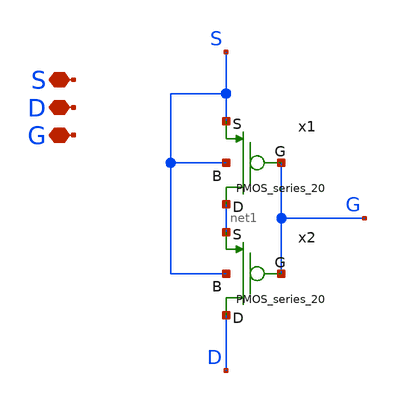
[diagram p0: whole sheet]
** sch_path: Voltage_Reference/symbols_vr/PMOS_series_20_2.sch
**.subckt PMOS_series_20_2 S D G
*.iopin S
*.iopin D
*.iopin G
x1 S net1 S G PMOS_series_20
x2 net1 D S G PMOS_series_20
**.ends

* expanding   symbol:  symbols_vr/PMOS_series_20.sym # of pins=4
** sym_path: Voltage_Reference/symbols_vr/PMOS_series_20.sym
** sch_path: Voltage_Reference/symbols_vr/PMOS_series_20.sch
.subckt PMOS_series_20 S D B G
*.iopin S
*.iopin D
*.iopin B
*.iopin G
XMP1 net1 G S B pfet_03v3 L=2u W=2u nf=1 ad='int((nf+1)/2) * W/nf * 0.18u' as='int((nf+2)/2) * W/nf * 0.18u'
+ pd='2*int((nf+1)/2) * (W/nf + 0.18u)' ps='2*int((nf+2)/2) * (W/nf + 0.18u)' nrd='0.18u / W' nrs='0.18u / W'
+ sa=0 sb=0 sd=0 m=1
XMP2 net3 G net1 B pfet_03v3 L=2u W=2u nf=1 ad='int((nf+1)/2) * W/nf * 0.18u' as='int((nf+2)/2) * W/nf * 0.18u'
+ pd='2*int((nf+1)/2) * (W/nf + 0.18u)' ps='2*int((nf+2)/2) * (W/nf + 0.18u)' nrd='0.18u / W' nrs='0.18u / W'
+ sa=0 sb=0 sd=0 m=1
XMP3 net2 G net3 B pfet_03v3 L=2u W=2u nf=1 ad='int((nf+1)/2) * W/nf * 0.18u' as='int((nf+2)/2) * W/nf * 0.18u'
+ pd='2*int((nf+1)/2) * (W/nf + 0.18u)' ps='2*int((nf+2)/2) * (W/nf + 0.18u)' nrd='0.18u / W' nrs='0.18u / W'
+ sa=0 sb=0 sd=0 m=1
XMP4 net5 G net2 B pfet_03v3 L=2u W=2u nf=1 ad='int((nf+1)/2) * W/nf * 0.18u' as='int((nf+2)/2) * W/nf * 0.18u'
+ pd='2*int((nf+1)/2) * (W/nf + 0.18u)' ps='2*int((nf+2)/2) * (W/nf + 0.18u)' nrd='0.18u / W' nrs='0.18u / W'
+ sa=0 sb=0 sd=0 m=1
XMP5 net4 G net5 B pfet_03v3 L=2u W=2u nf=1 ad='int((nf+1)/2) * W/nf * 0.18u' as='int((nf+2)/2) * W/nf * 0.18u'
+ pd='2*int((nf+1)/2) * (W/nf + 0.18u)' ps='2*int((nf+2)/2) * (W/nf + 0.18u)' nrd='0.18u / W' nrs='0.18u / W'
+ sa=0 sb=0 sd=0 m=1
XMP6 net7 G net4 B pfet_03v3 L=2u W=2u nf=1 ad='int((nf+1)/2) * W/nf * 0.18u' as='int((nf+2)/2) * W/nf * 0.18u'
+ pd='2*int((nf+1)/2) * (W/nf + 0.18u)' ps='2*int((nf+2)/2) * (W/nf + 0.18u)' nrd='0.18u / W' nrs='0.18u / W'
+ sa=0 sb=0 sd=0 m=1
XMP7 net6 G net7 B pfet_03v3 L=2u W=2u nf=1 ad='int((nf+1)/2) * W/nf * 0.18u' as='int((nf+2)/2) * W/nf * 0.18u'
+ pd='2*int((nf+1)/2) * (W/nf + 0.18u)' ps='2*int((nf+2)/2) * (W/nf + 0.18u)' nrd='0.18u / W' nrs='0.18u / W'
+ sa=0 sb=0 sd=0 m=1
XMP8 net9 G net6 B pfet_03v3 L=2u W=2u nf=1 ad='int((nf+1)/2) * W/nf * 0.18u' as='int((nf+2)/2) * W/nf * 0.18u'
+ pd='2*int((nf+1)/2) * (W/nf + 0.18u)' ps='2*int((nf+2)/2) * (W/nf + 0.18u)' nrd='0.18u / W' nrs='0.18u / W'
+ sa=0 sb=0 sd=0 m=1
XMP9 net8 G net9 B pfet_03v3 L=2u W=2u nf=1 ad='int((nf+1)/2) * W/nf * 0.18u' as='int((nf+2)/2) * W/nf * 0.18u'
+ pd='2*int((nf+1)/2) * (W/nf + 0.18u)' ps='2*int((nf+2)/2) * (W/nf + 0.18u)' nrd='0.18u / W' nrs='0.18u / W'
+ sa=0 sb=0 sd=0 m=1
XMP10 net19 G net8 B pfet_03v3 L=2u W=2u nf=1 ad='int((nf+1)/2) * W/nf * 0.18u' as='int((nf+2)/2) * W/nf * 0.18u'
+ pd='2*int((nf+1)/2) * (W/nf + 0.18u)' ps='2*int((nf+2)/2) * (W/nf + 0.18u)' nrd='0.18u / W' nrs='0.18u / W'
+ sa=0 sb=0 sd=0 m=1
XMP11 net10 G net19 B pfet_03v3 L=2u W=2u nf=1 ad='int((nf+1)/2) * W/nf * 0.18u' as='int((nf+2)/2) * W/nf * 0.18u'
+ pd='2*int((nf+1)/2) * (W/nf + 0.18u)' ps='2*int((nf+2)/2) * (W/nf + 0.18u)' nrd='0.18u / W' nrs='0.18u / W'
+ sa=0 sb=0 sd=0 m=1
XMP12 net12 G net10 B pfet_03v3 L=2u W=2u nf=1 ad='int((nf+1)/2) * W/nf * 0.18u' as='int((nf+2)/2) * W/nf * 0.18u'
+ pd='2*int((nf+1)/2) * (W/nf + 0.18u)' ps='2*int((nf+2)/2) * (W/nf + 0.18u)' nrd='0.18u / W' nrs='0.18u / W'
+ sa=0 sb=0 sd=0 m=1
XMP13 net11 G net12 B pfet_03v3 L=2u W=2u nf=1 ad='int((nf+1)/2) * W/nf * 0.18u' as='int((nf+2)/2) * W/nf * 0.18u'
+ pd='2*int((nf+1)/2) * (W/nf + 0.18u)' ps='2*int((nf+2)/2) * (W/nf + 0.18u)' nrd='0.18u / W' nrs='0.18u / W'
+ sa=0 sb=0 sd=0 m=1
XMP14 net14 G net11 B pfet_03v3 L=2u W=2u nf=1 ad='int((nf+1)/2) * W/nf * 0.18u' as='int((nf+2)/2) * W/nf * 0.18u'
+ pd='2*int((nf+1)/2) * (W/nf + 0.18u)' ps='2*int((nf+2)/2) * (W/nf + 0.18u)' nrd='0.18u / W' nrs='0.18u / W'
+ sa=0 sb=0 sd=0 m=1
XMP15 net13 G net14 B pfet_03v3 L=2u W=2u nf=1 ad='int((nf+1)/2) * W/nf * 0.18u' as='int((nf+2)/2) * W/nf * 0.18u'
+ pd='2*int((nf+1)/2) * (W/nf + 0.18u)' ps='2*int((nf+2)/2) * (W/nf + 0.18u)' nrd='0.18u / W' nrs='0.18u / W'
+ sa=0 sb=0 sd=0 m=1
XMP16 net16 G net13 B pfet_03v3 L=2u W=2u nf=1 ad='int((nf+1)/2) * W/nf * 0.18u' as='int((nf+2)/2) * W/nf * 0.18u'
+ pd='2*int((nf+1)/2) * (W/nf + 0.18u)' ps='2*int((nf+2)/2) * (W/nf + 0.18u)' nrd='0.18u / W' nrs='0.18u / W'
+ sa=0 sb=0 sd=0 m=1
XMP17 net15 G net16 B pfet_03v3 L=2u W=2u nf=1 ad='int((nf+1)/2) * W/nf * 0.18u' as='int((nf+2)/2) * W/nf * 0.18u'
+ pd='2*int((nf+1)/2) * (W/nf + 0.18u)' ps='2*int((nf+2)/2) * (W/nf + 0.18u)' nrd='0.18u / W' nrs='0.18u / W'
+ sa=0 sb=0 sd=0 m=1
XMP18 net18 G net15 B pfet_03v3 L=2u W=2u nf=1 ad='int((nf+1)/2) * W/nf * 0.18u' as='int((nf+2)/2) * W/nf * 0.18u'
+ pd='2*int((nf+1)/2) * (W/nf + 0.18u)' ps='2*int((nf+2)/2) * (W/nf + 0.18u)' nrd='0.18u / W' nrs='0.18u / W'
+ sa=0 sb=0 sd=0 m=1
XMP19 net17 G net18 B pfet_03v3 L=2u W=2u nf=1 ad='int((nf+1)/2) * W/nf * 0.18u' as='int((nf+2)/2) * W/nf * 0.18u'
+ pd='2*int((nf+1)/2) * (W/nf + 0.18u)' ps='2*int((nf+2)/2) * (W/nf + 0.18u)' nrd='0.18u / W' nrs='0.18u / W'
+ sa=0 sb=0 sd=0 m=1
XMP20 D G net17 B pfet_03v3 L=2u W=2u nf=1 ad='int((nf+1)/2) * W/nf * 0.18u' as='int((nf+2)/2) * W/nf * 0.18u'
+ pd='2*int((nf+1)/2) * (W/nf + 0.18u)' ps='2*int((nf+2)/2) * (W/nf + 0.18u)' nrd='0.18u / W' nrs='0.18u / W'
+ sa=0 sb=0 sd=0 m=1
XMP21[1] B B B B pfet_03v3 L=2u W=2u nf=1 ad='int((nf+1)/2) * W/nf * 0.18u' as='int((nf+2)/2) * W/nf * 0.18u'
+ pd='2*int((nf+1)/2) * (W/nf + 0.18u)' ps='2*int((nf+2)/2) * (W/nf + 0.18u)' nrd='0.18u / W' nrs='0.18u / W'
+ sa=0 sb=0 sd=0 m=1
XMP21[2] B B B B pfet_03v3 L=2u W=2u nf=1 ad='int((nf+1)/2) * W/nf * 0.18u' as='int((nf+2)/2) * W/nf * 0.18u'
+ pd='2*int((nf+1)/2) * (W/nf + 0.18u)' ps='2*int((nf+2)/2) * (W/nf + 0.18u)' nrd='0.18u / W' nrs='0.18u / W'
+ sa=0 sb=0 sd=0 m=1
XMP21[3] B B B B pfet_03v3 L=2u W=2u nf=1 ad='int((nf+1)/2) * W/nf * 0.18u' as='int((nf+2)/2) * W/nf * 0.18u'
+ pd='2*int((nf+1)/2) * (W/nf + 0.18u)' ps='2*int((nf+2)/2) * (W/nf + 0.18u)' nrd='0.18u / W' nrs='0.18u / W'
+ sa=0 sb=0 sd=0 m=1
XMP21[4] B B B B pfet_03v3 L=2u W=2u nf=1 ad='int((nf+1)/2) * W/nf * 0.18u' as='int((nf+2)/2) * W/nf * 0.18u'
+ pd='2*int((nf+1)/2) * (W/nf + 0.18u)' ps='2*int((nf+2)/2) * (W/nf + 0.18u)' nrd='0.18u / W' nrs='0.18u / W'
+ sa=0 sb=0 sd=0 m=1
XMP21[5] B B B B pfet_03v3 L=2u W=2u nf=1 ad='int((nf+1)/2) * W/nf * 0.18u' as='int((nf+2)/2) * W/nf * 0.18u'
+ pd='2*int((nf+1)/2) * (W/nf + 0.18u)' ps='2*int((nf+2)/2) * (W/nf + 0.18u)' nrd='0.18u / W' nrs='0.18u / W'
+ sa=0 sb=0 sd=0 m=1
XMP21[6] B B B B pfet_03v3 L=2u W=2u nf=1 ad='int((nf+1)/2) * W/nf * 0.18u' as='int((nf+2)/2) * W/nf * 0.18u'
+ pd='2*int((nf+1)/2) * (W/nf + 0.18u)' ps='2*int((nf+2)/2) * (W/nf + 0.18u)' nrd='0.18u / W' nrs='0.18u / W'
+ sa=0 sb=0 sd=0 m=1
XMP21[7] B B B B pfet_03v3 L=2u W=2u nf=1 ad='int((nf+1)/2) * W/nf * 0.18u' as='int((nf+2)/2) * W/nf * 0.18u'
+ pd='2*int((nf+1)/2) * (W/nf + 0.18u)' ps='2*int((nf+2)/2) * (W/nf + 0.18u)' nrd='0.18u / W' nrs='0.18u / W'
+ sa=0 sb=0 sd=0 m=1
XMP21[8] B B B B pfet_03v3 L=2u W=2u nf=1 ad='int((nf+1)/2) * W/nf * 0.18u' as='int((nf+2)/2) * W/nf * 0.18u'
+ pd='2*int((nf+1)/2) * (W/nf + 0.18u)' ps='2*int((nf+2)/2) * (W/nf + 0.18u)' nrd='0.18u / W' nrs='0.18u / W'
+ sa=0 sb=0 sd=0 m=1
XMP21[9] B B B B pfet_03v3 L=2u W=2u nf=1 ad='int((nf+1)/2) * W/nf * 0.18u' as='int((nf+2)/2) * W/nf * 0.18u'
+ pd='2*int((nf+1)/2) * (W/nf + 0.18u)' ps='2*int((nf+2)/2) * (W/nf + 0.18u)' nrd='0.18u / W' nrs='0.18u / W'
+ sa=0 sb=0 sd=0 m=1
XMP21[10] B B B B pfet_03v3 L=2u W=2u nf=1 ad='int((nf+1)/2) * W/nf * 0.18u' as='int((nf+2)/2) * W/nf * 0.18u'
+ pd='2*int((nf+1)/2) * (W/nf + 0.18u)' ps='2*int((nf+2)/2) * (W/nf + 0.18u)' nrd='0.18u / W' nrs='0.18u / W'
+ sa=0 sb=0 sd=0 m=1
XMP21[11] B B B B pfet_03v3 L=2u W=2u nf=1 ad='int((nf+1)/2) * W/nf * 0.18u' as='int((nf+2)/2) * W/nf * 0.18u'
+ pd='2*int((nf+1)/2) * (W/nf + 0.18u)' ps='2*int((nf+2)/2) * (W/nf + 0.18u)' nrd='0.18u / W' nrs='0.18u / W'
+ sa=0 sb=0 sd=0 m=1
XMP21[12] B B B B pfet_03v3 L=2u W=2u nf=1 ad='int((nf+1)/2) * W/nf * 0.18u' as='int((nf+2)/2) * W/nf * 0.18u'
+ pd='2*int((nf+1)/2) * (W/nf + 0.18u)' ps='2*int((nf+2)/2) * (W/nf + 0.18u)' nrd='0.18u / W' nrs='0.18u / W'
+ sa=0 sb=0 sd=0 m=1
XMP21[13] B B B B pfet_03v3 L=2u W=2u nf=1 ad='int((nf+1)/2) * W/nf * 0.18u' as='int((nf+2)/2) * W/nf * 0.18u'
+ pd='2*int((nf+1)/2) * (W/nf + 0.18u)' ps='2*int((nf+2)/2) * (W/nf + 0.18u)' nrd='0.18u / W' nrs='0.18u / W'
+ sa=0 sb=0 sd=0 m=1
XMP21[14] B B B B pfet_03v3 L=2u W=2u nf=1 ad='int((nf+1)/2) * W/nf * 0.18u' as='int((nf+2)/2) * W/nf * 0.18u'
+ pd='2*int((nf+1)/2) * (W/nf + 0.18u)' ps='2*int((nf+2)/2) * (W/nf + 0.18u)' nrd='0.18u / W' nrs='0.18u / W'
+ sa=0 sb=0 sd=0 m=1
XMP21[15] B B B B pfet_03v3 L=2u W=2u nf=1 ad='int((nf+1)/2) * W/nf * 0.18u' as='int((nf+2)/2) * W/nf * 0.18u'
+ pd='2*int((nf+1)/2) * (W/nf + 0.18u)' ps='2*int((nf+2)/2) * (W/nf + 0.18u)' nrd='0.18u / W' nrs='0.18u / W'
+ sa=0 sb=0 sd=0 m=1
XMP21[16] B B B B pfet_03v3 L=2u W=2u nf=1 ad='int((nf+1)/2) * W/nf * 0.18u' as='int((nf+2)/2) * W/nf * 0.18u'
+ pd='2*int((nf+1)/2) * (W/nf + 0.18u)' ps='2*int((nf+2)/2) * (W/nf + 0.18u)' nrd='0.18u / W' nrs='0.18u / W'
+ sa=0 sb=0 sd=0 m=1
XMP21[17] B B B B pfet_03v3 L=2u W=2u nf=1 ad='int((nf+1)/2) * W/nf * 0.18u' as='int((nf+2)/2) * W/nf * 0.18u'
+ pd='2*int((nf+1)/2) * (W/nf + 0.18u)' ps='2*int((nf+2)/2) * (W/nf + 0.18u)' nrd='0.18u / W' nrs='0.18u / W'
+ sa=0 sb=0 sd=0 m=1
XMP21[18] B B B B pfet_03v3 L=2u W=2u nf=1 ad='int((nf+1)/2) * W/nf * 0.18u' as='int((nf+2)/2) * W/nf * 0.18u'
+ pd='2*int((nf+1)/2) * (W/nf + 0.18u)' ps='2*int((nf+2)/2) * (W/nf + 0.18u)' nrd='0.18u / W' nrs='0.18u / W'
+ sa=0 sb=0 sd=0 m=1
XMP21[19] B B B B pfet_03v3 L=2u W=2u nf=1 ad='int((nf+1)/2) * W/nf * 0.18u' as='int((nf+2)/2) * W/nf * 0.18u'
+ pd='2*int((nf+1)/2) * (W/nf + 0.18u)' ps='2*int((nf+2)/2) * (W/nf + 0.18u)' nrd='0.18u / W' nrs='0.18u / W'
+ sa=0 sb=0 sd=0 m=1
XMP21[20] B B B B pfet_03v3 L=2u W=2u nf=1 ad='int((nf+1)/2) * W/nf * 0.18u' as='int((nf+2)/2) * W/nf * 0.18u'
+ pd='2*int((nf+1)/2) * (W/nf + 0.18u)' ps='2*int((nf+2)/2) * (W/nf + 0.18u)' nrd='0.18u / W' nrs='0.18u / W'
+ sa=0 sb=0 sd=0 m=1
XMP21[21] B B B B pfet_03v3 L=2u W=2u nf=1 ad='int((nf+1)/2) * W/nf * 0.18u' as='int((nf+2)/2) * W/nf * 0.18u'
+ pd='2*int((nf+1)/2) * (W/nf + 0.18u)' ps='2*int((nf+2)/2) * (W/nf + 0.18u)' nrd='0.18u / W' nrs='0.18u / W'
+ sa=0 sb=0 sd=0 m=1
XMP21[22] B B B B pfet_03v3 L=2u W=2u nf=1 ad='int((nf+1)/2) * W/nf * 0.18u' as='int((nf+2)/2) * W/nf * 0.18u'
+ pd='2*int((nf+1)/2) * (W/nf + 0.18u)' ps='2*int((nf+2)/2) * (W/nf + 0.18u)' nrd='0.18u / W' nrs='0.18u / W'
+ sa=0 sb=0 sd=0 m=1
.ends

.end
